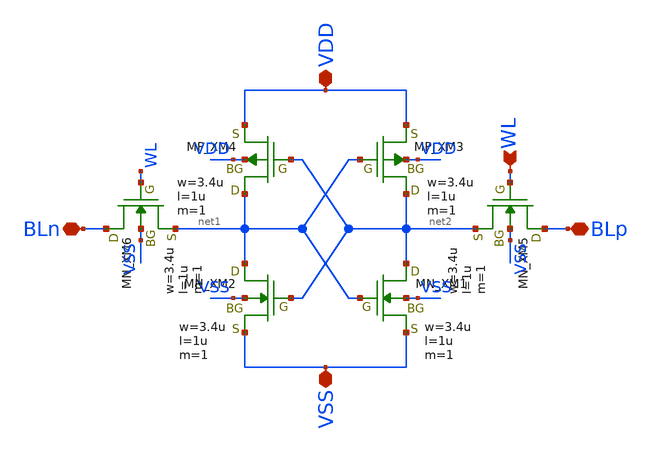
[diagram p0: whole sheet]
** sch_path: module/SRAM128/schematic/BIT_CELL.sch
**.subckt BIT_CELL VDD VSS WL BLp BLn
*.iopin VDD
*.iopin VSS
*.ipin WL
*.iopin BLp
*.iopin BLn
XXM1 net2 net1 VSS VSS NMOS w=3.4u l=1u as=0 ad=0 ps=0 pd=0 nrd=0 nrs=0 m=1
XXM2 net1 net2 VSS VSS NMOS w=3.4u l=1u as=0 ad=0 ps=0 pd=0 nrd=0 nrs=0 m=1
XXM3 net2 net1 VDD VDD PMOS w=3.4u l=1u as=0 ad=0 ps=0 pd=0 nrd=0 nrs=0 m=1
XXM4 net1 net2 VDD VDD PMOS w=3.4u l=1u as=0 ad=0 ps=0 pd=0 nrd=0 nrs=0 m=1
XXM5 BLp WL net2 VSS NMOS w=3.4u l=1u as=0 ad=0 ps=0 pd=0 nrd=0 nrs=0 m=1
XXM6 BLn WL net1 VSS NMOS w=3.4u l=1u as=0 ad=0 ps=0 pd=0 nrd=0 nrs=0 m=1
**.ends
.end
